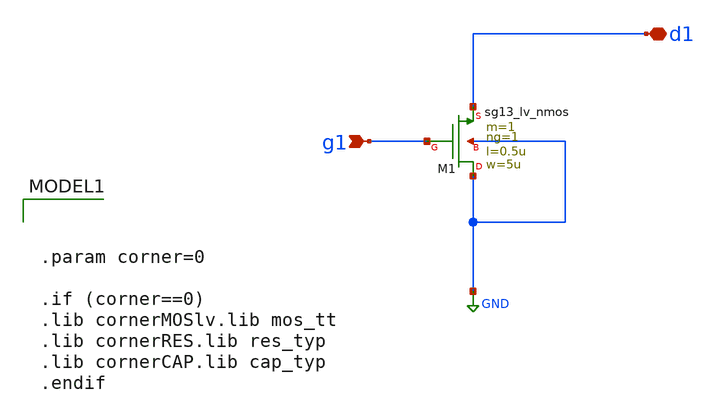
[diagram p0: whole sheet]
** sch_path: Tarea_1/xschem/nmoslv_charac_IPD413-202501-HW1.sch
**.subckt nmoslv_charac_IPD413-202501-HW1 g1 d1
*.ipin g1
*.iopin d1
XM1 GND g1 d1 GND sg13_lv_nmos w=5u l=0.5u ng=1 m=1 mm_ok=1
**** begin user architecture code


.param corner=0

.if (corner==0)
.lib cornerMOSlv.lib mos_tt
.lib cornerRES.lib res_typ
.lib cornerCAP.lib cap_typ
.endif



.param vd = 0.75
.param vg = 0.75

vgs g1 0 {vd}
vds d1 0 {vg}
.control
save all
save @n.xm1.nsg13_lv_nmos[ids]
save @n.xm1.nsg13_lv_nmos[gm]
save @n.xm1.nsg13_lv_nmos[vth]
save @n.xm1.nsg13_lv_nmos[cgg]
save @n.xm1.nsg13_lv_nmos[cgsol]
save @n.xm1.nsg13_lv_nmos[cgdol]
save @n.xm1.nsg13_lv_nmos[vgs]
save @n.xm1.nsg13_lv_nmos[vdss]

dc vgs 0.01 1.8 0.01 vds 0.4 1.35 0.05

let idn = @n.xm1.nsg13_lv_nmos[ids]
let gmn = @n.xm1.nsg13_lv_nmos[gm]
let vthn = @n.xm1.nsg13_lv_nmos[vth]
let vgsn = @n.xm1.nsg13_lv_nmos[vgs]
let vdsatn = @n.xm1.nsg13_lv_nmos[vdss]

let cgg = @n.xm1.nsg13_lv_nmos[cgg]
let cgsol = @n.xm1.nsg13_lv_nmos[cgsol]
let cgdol = @n.xm1.nsg13_lv_nmos[cgdol]
let c_tot = cgg + cgsol + cgdol
let ft = gmn/(2*pi*c_tot)

let vov = 2*idn/gmn
let gmoverId = gmn/idn

wrdata nmos_char_idn.raw idn

wrdata nmos_char_gmid-ft.raw gmoverId ft

print vthn[0]
** Pregunta 1b
dc vds 0.0 1.35 0.01 vgs 0.4 1.5 0.1
let idn = @n.xm1.nsg13_lv_nmos[ids]
wrdata nmos_char_vds.raw idn

dc vgs 0.0 1.5 0.01
let idn = @n.xm1.nsg13_lv_nmos[ids]
wrdata nmos_char_1d.raw idn

.endc


**** end user architecture code
**.ends
.GLOBAL GND
.end
